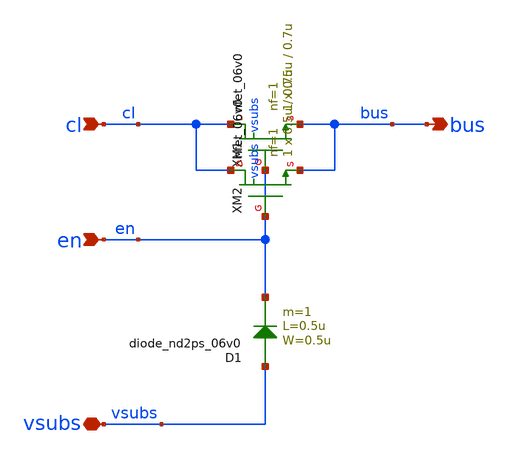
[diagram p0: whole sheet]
** sch_path: xschem/ip_column_switch.sch
**.subckt ip_column_switch cl en vsubs bus
*.ipin cl
*.ipin en
*.iopin vsubs
*.opin bus
XM1 cl en bus vsubs nfet_06v0 L=0.7u W=0.5u nf=1 ad='int((nf+1)/2) * W/nf * 0.18u' as='int((nf+2)/2) * W/nf * 0.18u'
+ pd='2*int((nf+1)/2) * (W/nf + 0.18u)' ps='2*int((nf+2)/2) * (W/nf + 0.18u)' nrd='0.18u / W' nrs='0.18u / W'
+ sa=0 sb=0 sd=0 m=1 par=1
D1 vsubs en diode_nd2ps_06v0 area='0.5u * 0.5u ' pj='2*0.5u + 2*0.5u ' m=1
XM2 cl en bus vsubs nfet_06v0 L=0.7u W=0.5u nf=1 ad='int((nf+1)/2) * W/nf * 0.18u' as='int((nf+2)/2) * W/nf * 0.18u'
+ pd='2*int((nf+1)/2) * (W/nf + 0.18u)' ps='2*int((nf+2)/2) * (W/nf + 0.18u)' nrd='0.18u / W' nrs='0.18u / W'
+ sa=0 sb=0 sd=0 m=1 par=1
**.ends
.end
